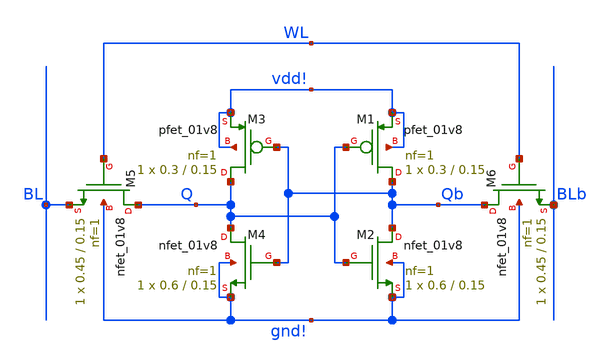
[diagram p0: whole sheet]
** sch_path: 6t_sram_130.sch
**.subckt 6t_sram_130
XM2 Qb Q gnd! gnd! sky130_fd_pr__nfet_01v8 L=0.15 W=0.6 nf=1 ad='int((nf+1)/2) * W/nf * 0.29' as='int((nf+2)/2) * W/nf * 0.29'
+ pd='2*int((nf+1)/2) * (W/nf + 0.29)' ps='2*int((nf+2)/2) * (W/nf + 0.29)' nrd='0.29 / W' nrs='0.29 / W'
+ sa=0 sb=0 sd=0 mult=1 m=1
XM4 Q Qb gnd! gnd! sky130_fd_pr__nfet_01v8 L=0.15 W=0.6 nf=1 ad='int((nf+1)/2) * W/nf * 0.29' as='int((nf+2)/2) * W/nf * 0.29'
+ pd='2*int((nf+1)/2) * (W/nf + 0.29)' ps='2*int((nf+2)/2) * (W/nf + 0.29)' nrd='0.29 / W' nrs='0.29 / W'
+ sa=0 sb=0 sd=0 mult=1 m=1
XM5 Q WL BL gnd! sky130_fd_pr__nfet_01v8 L=0.15 W=0.45 nf=1 ad='int((nf+1)/2) * W/nf * 0.29' as='int((nf+2)/2) * W/nf * 0.29'
+ pd='2*int((nf+1)/2) * (W/nf + 0.29)' ps='2*int((nf+2)/2) * (W/nf + 0.29)' nrd='0.29 / W' nrs='0.29 / W'
+ sa=0 sb=0 sd=0 mult=1 m=1
XM6 Qb WL BLb gnd! sky130_fd_pr__nfet_01v8 L=0.15 W=0.45 nf=1 ad='int((nf+1)/2) * W/nf * 0.29' as='int((nf+2)/2) * W/nf * 0.29'
+ pd='2*int((nf+1)/2) * (W/nf + 0.29)' ps='2*int((nf+2)/2) * (W/nf + 0.29)' nrd='0.29 / W' nrs='0.29 / W'
+ sa=0 sb=0 sd=0 mult=1 m=1
XM1 Qb Q vdd! vdd! sky130_fd_pr__pfet_01v8 L=0.15 W=0.3 nf=1 ad='int((nf+1)/2) * W/nf * 0.29' as='int((nf+2)/2) * W/nf * 0.29'
+ pd='2*int((nf+1)/2) * (W/nf + 0.29)' ps='2*int((nf+2)/2) * (W/nf + 0.29)' nrd='0.29 / W' nrs='0.29 / W'
+ sa=0 sb=0 sd=0 mult=1 m=1
XM3 Q Qb vdd! vdd! sky130_fd_pr__pfet_01v8 L=0.15 W=0.3 nf=1 ad='int((nf+1)/2) * W/nf * 0.29' as='int((nf+2)/2) * W/nf * 0.29'
+ pd='2*int((nf+1)/2) * (W/nf + 0.29)' ps='2*int((nf+2)/2) * (W/nf + 0.29)' nrd='0.29 / W' nrs='0.29 / W'
+ sa=0 sb=0 sd=0 mult=1 m=1
**.ends
.end
